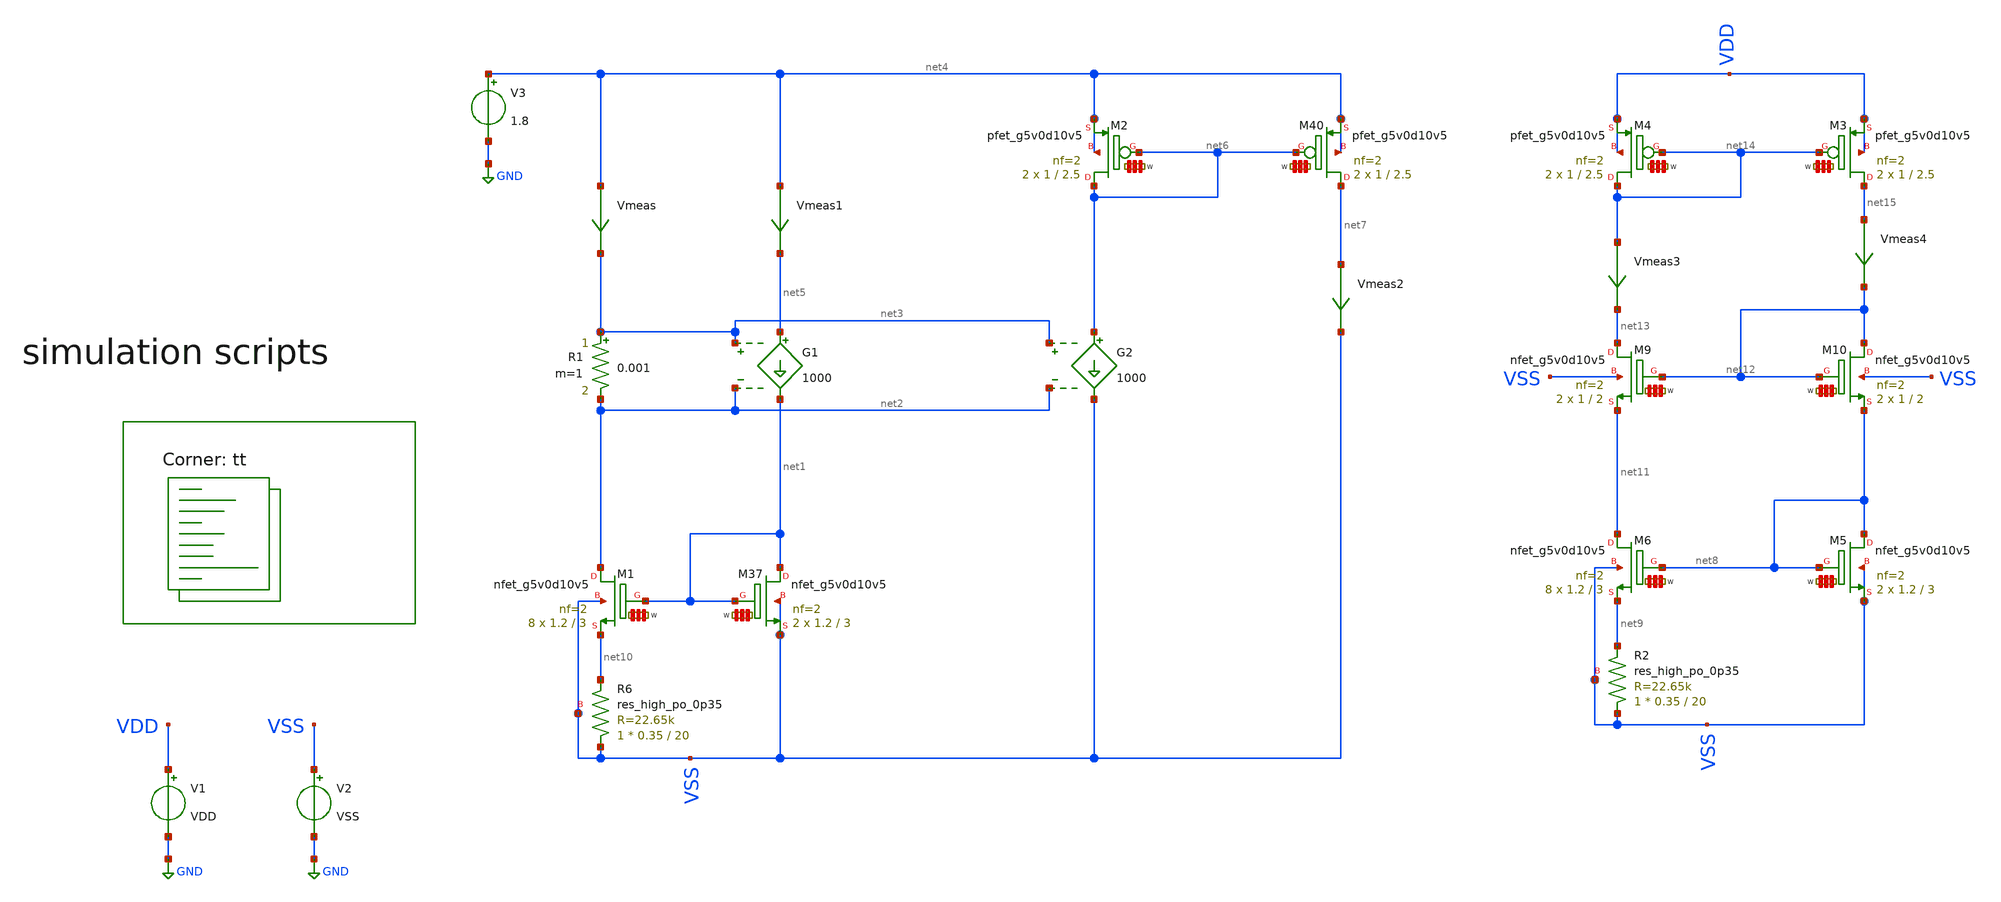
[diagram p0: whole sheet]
** sch_path: Learning/single_ended_amplifiers/Design_and_Analysis_of_Two-Stage_CMOS_Operational_Amplifier_for_Fluorescence_Signal_Processing_sky130_5V/transimpedance_cell_design/transcondutance_cell_design.sch
**.subckt transcondutance_cell_design
V1 VDD GND VDD
V2 VSS GND VSS
XR6 VSS net10 VSS sky130_fd_pr__res_high_po_0p35 L=20 mult=1 m=1
R1 net3 net2 0.001 m=1
G1 net5 net1 net3 net2 1000
Vmeas net4 net3 0
.save i(vmeas)
Vmeas1 net4 net5 0
.save i(vmeas1)
V3 net4 GND 1.8
G2 net6 VSS net3 net2 1000
Vmeas2 net7 VSS 0
.save i(vmeas2)
Vmeas3 net14 net13 0
.save i(vmeas3)
Vmeas4 net15 net12 0
.save i(vmeas4)
XM9 net13 net12 net11 VSS sky130_fd_pr__nfet_g5v0d10v5 L=2 W='1 * 2 ' nf=2 ad='int((nf+1)/2) * W / nf * 0.29'
+ as='int((nf+2)/2) * W / nf * 0.29' pd='2*int((nf+1)/2) * (W / nf + 0.29)' ps='2*int((nf+2)/2) * (W / nf + 0.29)'
+ nrd='0.29 / W ' nrs='0.29 / W ' sa=0 sb=0 sd=0 mult=2 m=2
XM10 net12 net12 net8 VSS sky130_fd_pr__nfet_g5v0d10v5 L=2 W='1 * 2 ' nf=2 ad='int((nf+1)/2) * W / nf * 0.29'
+ as='int((nf+2)/2) * W / nf * 0.29' pd='2*int((nf+1)/2) * (W / nf + 0.29)' ps='2*int((nf+2)/2) * (W / nf + 0.29)'
+ nrd='0.29 / W ' nrs='0.29 / W ' sa=0 sb=0 sd=0 mult=2 m=2
XM37 net1 net1 VSS VSS sky130_fd_pr__nfet_g5v0d10v5 L=3 W='1.2 * 2 ' nf=2 ad='int((nf+1)/2) * W / nf * 0.29'
+ as='int((nf+2)/2) * W / nf * 0.29' pd='2*int((nf+1)/2) * (W / nf + 0.29)' ps='2*int((nf+2)/2) * (W / nf + 0.29)'
+ nrd='0.29 / W ' nrs='0.29 / W ' sa=0 sb=0 sd=0 mult=2 m=2
XM1 net2 net1 net10 VSS sky130_fd_pr__nfet_g5v0d10v5 L=3 W='1.2 * 2 ' nf=2 ad='int((nf+1)/2) * W / nf * 0.29'
+ as='int((nf+2)/2) * W / nf * 0.29' pd='2*int((nf+1)/2) * (W / nf + 0.29)' ps='2*int((nf+2)/2) * (W / nf + 0.29)'
+ nrd='0.29 / W ' nrs='0.29 / W ' sa=0 sb=0 sd=0 mult=8 m=8
XM40 net7 net6 net4 net4 sky130_fd_pr__pfet_g5v0d10v5 L=2.5 W='1 * 2 ' nf=2 ad='int((2 + 1)/2) * 1 * 0.29'
+ as='int((2 + 2)/2) * 1 * 0.29' pd='2*int((2 + 1)/2) * (1 + 0.29)' ps='2*int((2 + 2)/2) * (1 + 0.29)'
+ nrd='0.29 / 1 / 2 ' nrs='0.29 / 1 / 2 ' sa=0 sb=0 sd=0 mult=2 m=2
XM2 net6 net6 net4 net4 sky130_fd_pr__pfet_g5v0d10v5 L=2.5 W='1 * 2 ' nf=2 ad='int((2 + 1)/2) * 1 * 0.29'
+ as='int((2 + 2)/2) * 1 * 0.29' pd='2*int((2 + 1)/2) * (1 + 0.29)' ps='2*int((2 + 2)/2) * (1 + 0.29)'
+ nrd='0.29 / 1 / 2 ' nrs='0.29 / 1 / 2 ' sa=0 sb=0 sd=0 mult=2 m=2
XM3 net15 net14 VDD VDD sky130_fd_pr__pfet_g5v0d10v5 L=2.5 W='1 * 2 ' nf=2 ad='int((2 + 1)/2) * 1 * 0.29'
+ as='int((2 + 2)/2) * 1 * 0.29' pd='2*int((2 + 1)/2) * (1 + 0.29)' ps='2*int((2 + 2)/2) * (1 + 0.29)'
+ nrd='0.29 / 1 / 2 ' nrs='0.29 / 1 / 2 ' sa=0 sb=0 sd=0 mult=2 m=2
XM4 net14 net14 VDD VDD sky130_fd_pr__pfet_g5v0d10v5 L=2.5 W='1 * 2 ' nf=2 ad='int((2 + 1)/2) * 1 * 0.29'
+ as='int((2 + 2)/2) * 1 * 0.29' pd='2*int((2 + 1)/2) * (1 + 0.29)' ps='2*int((2 + 2)/2) * (1 + 0.29)'
+ nrd='0.29 / 1 / 2 ' nrs='0.29 / 1 / 2 ' sa=0 sb=0 sd=0 mult=2 m=2
XM5 net8 net8 VSS VSS sky130_fd_pr__nfet_g5v0d10v5 L=3 W='1.2 * 2 ' nf=2 ad='int((nf+1)/2) * W / nf * 0.29'
+ as='int((nf+2)/2) * W / nf * 0.29' pd='2*int((nf+1)/2) * (W / nf + 0.29)' ps='2*int((nf+2)/2) * (W / nf + 0.29)'
+ nrd='0.29 / W ' nrs='0.29 / W ' sa=0 sb=0 sd=0 mult=2 m=2
XM6 net11 net8 net9 VSS sky130_fd_pr__nfet_g5v0d10v5 L=3 W='1.2 * 2 ' nf=2 ad='int((nf+1)/2) * W / nf * 0.29'
+ as='int((nf+2)/2) * W / nf * 0.29' pd='2*int((nf+1)/2) * (W / nf + 0.29)' ps='2*int((nf+2)/2) * (W / nf + 0.29)'
+ nrd='0.29 / W ' nrs='0.29 / W ' sa=0 sb=0 sd=0 mult=8 m=8
XR2 VSS net9 VSS sky130_fd_pr__res_high_po_0p35 L=20 mult=1 m=1
**** begin user architecture code
.lib $::SKYWATER_MODELS/sky130.lib.spice tt


.Temp 27
.param VDD = 5
.param VSS = 0


.control
save all

save @m.xm2.msky130_fd_pr__nfet_g5v0d10v5[vdsat]

dc Temp -40 125 1
*plot i(Vmeas) i(Vmeas2)
plot i(Vmeas1) i(Vmeas2)
plot i(Vmeas3) i(Vmeas4)
wrdata data.csv i(Vmeas3) i(Vmeas4)


op
print i(Vmeas1)
print v(net2)




.endc

**** end user architecture code
**.ends
.GLOBAL GND
.end
